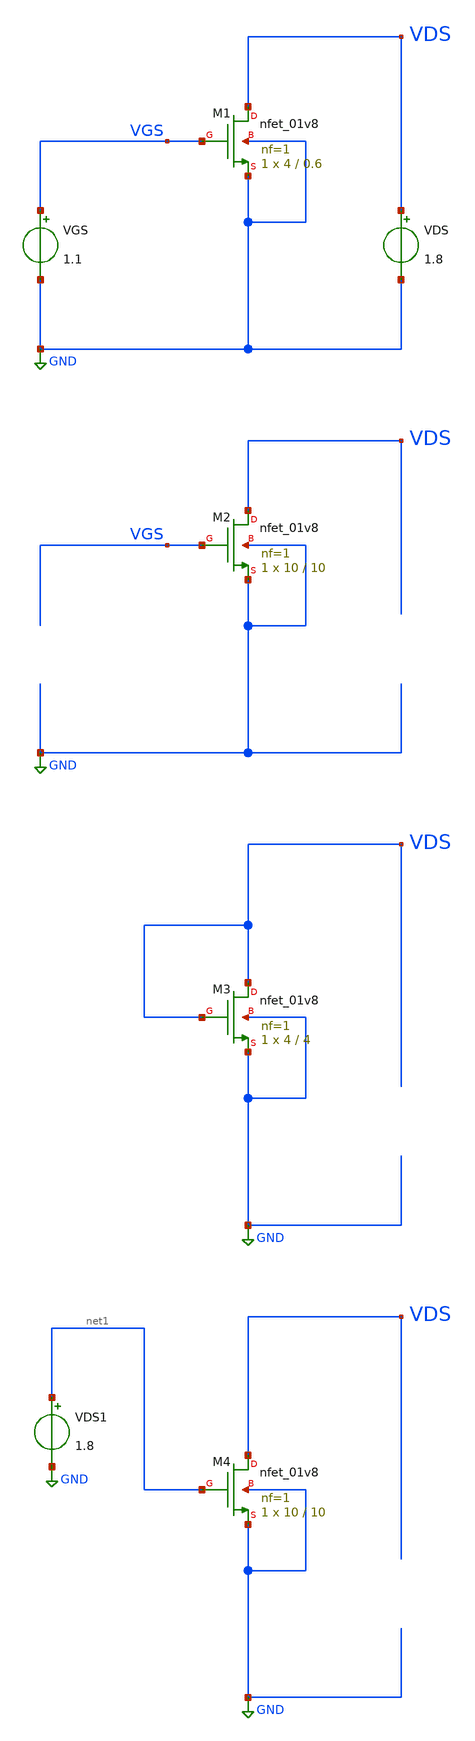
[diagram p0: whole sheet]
** sch_path: projects/bandgapref/xschem_ngspice/new_files/vgs_id_sweep_nfet.sch
**.subckt vgs_id_sweep_nfet
XM1 VDS VGS GND GND sky130_fd_pr__nfet_01v8 L=0.6 W=4 nf=1 ad='int((nf+1)/2) * W/nf * 0.29' as='int((nf+2)/2) * W/nf * 0.29'
+ pd='2*int((nf+1)/2) * (W/nf + 0.29)' ps='2*int((nf+2)/2) * (W/nf + 0.29)' nrd='0.29 / W' nrs='0.29 / W'
+ sa=0 sb=0 sd=0 mult=1 m=1
VGS VGS GND 1.1
VDS VDS GND 1.8
XM2 VDS VGS GND GND sky130_fd_pr__nfet_01v8 L=10 W=10 nf=1 ad='int((nf+1)/2) * W/nf * 0.29' as='int((nf+2)/2) * W/nf * 0.29'
+ pd='2*int((nf+1)/2) * (W/nf + 0.29)' ps='2*int((nf+2)/2) * (W/nf + 0.29)' nrd='0.29 / W' nrs='0.29 / W'
+ sa=0 sb=0 sd=0 mult=1 m=1
XM3 VDS VDS GND GND sky130_fd_pr__nfet_01v8 L=4 W=4 nf=1 ad='int((nf+1)/2) * W/nf * 0.29' as='int((nf+2)/2) * W/nf * 0.29'
+ pd='2*int((nf+1)/2) * (W/nf + 0.29)' ps='2*int((nf+2)/2) * (W/nf + 0.29)' nrd='0.29 / W' nrs='0.29 / W'
+ sa=0 sb=0 sd=0 mult=1 m=1
XM4 VDS net1 GND GND sky130_fd_pr__nfet_01v8 L=10 W=10 nf=1 ad='int((nf+1)/2) * W/nf * 0.29' as='int((nf+2)/2) * W/nf * 0.29'
+ pd='2*int((nf+1)/2) * (W/nf + 0.29)' ps='2*int((nf+2)/2) * (W/nf + 0.29)' nrd='0.29 / W' nrs='0.29 / W'
+ sa=0 sb=0 sd=0 mult=1 m=1
VDS1 net1 GND 1.8
**** begin user architecture code
.lib $::SKYWATER_MODELS/sky130.lib.spice tt



.option method=gear
.option wnflag=1
.option savecurrents

.save @m.xm1.msky130_fd_pr__nfet_01v8[gm] @m.xm2.msky130_fd_pr__nfet_01v8[gm] @m.xm3.msky130_fd_pr__nfet_01v8[gm] @m.xm4.msky130_fd_pr__nfet_01v8[gm]

.control
  save all
  *  dc VGS 0 1.8 0.1 VDS 0 1.8 0.1
  dc VDS 0 1.8 0.001 VGS 0 1.8 0.05
  remzerovec
  write vgs_id_sweep_nfet.raw
  set appendwrite
.endc



**** end user architecture code
**.ends
.GLOBAL GND
.end
